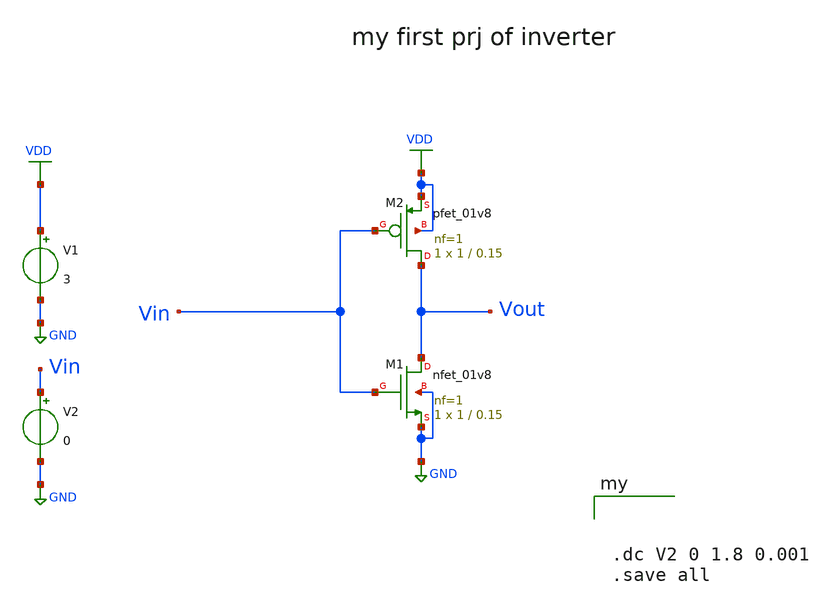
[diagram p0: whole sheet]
** sch_path: Sky130 xsch magic/xscheme/inverter_xsheme.sch
**.subckt inverter_xsheme
XM1 Vout Vin GND GND sky130_fd_pr__nfet_01v8 L=0.15 W=1 nf=1 ad='int((nf+1)/2) * W/nf * 0.29' as='int((nf+2)/2) * W/nf * 0.29'
+ pd='2*int((nf+1)/2) * (W/nf + 0.29)' ps='2*int((nf+2)/2) * (W/nf + 0.29)' nrd='0.29 / W' nrs='0.29 / W'
+ sa=0 sb=0 sd=0 mult=1 m=1
XM2 Vout Vin VDD VDD sky130_fd_pr__pfet_01v8 L=0.15 W=1 nf=1 ad='int((nf+1)/2) * W/nf * 0.29' as='int((nf+2)/2) * W/nf * 0.29'
+ pd='2*int((nf+1)/2) * (W/nf + 0.29)' ps='2*int((nf+2)/2) * (W/nf + 0.29)' nrd='0.29 / W' nrs='0.29 / W'
+ sa=0 sb=0 sd=0 mult=1 m=1
V2 Vin GND 0
V1 VDD GND 3
**** begin user architecture code



.lib /usr/local/share/xschem/xschem_library/devices/sky130A/libs.tech/ngspice/sky130.lib.spice tt




.dc V2 0 1.8 0.001
.save all



**** end user architecture code
**.ends
.GLOBAL VDD
.GLOBAL GND
.end
